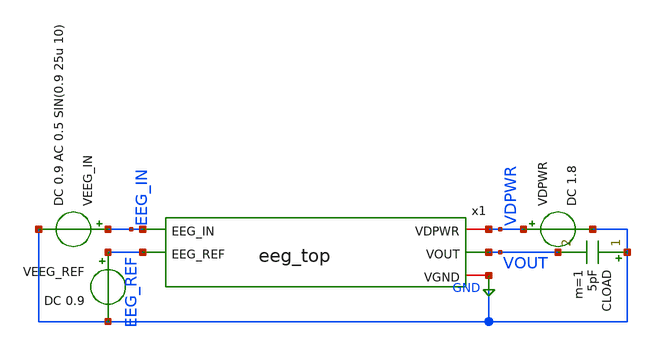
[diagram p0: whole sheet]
** sch_path: xschem/tb_eeg_top.sch
**.subckt tb_eeg_top
VDPWR VDPWR GND DC 1.8
VEEG_REF EEG_REF GND DC 0.9
VEEG_IN EEG_IN GND DC 0.9 AC 0.5 SIN(0.9 25u 10)
CLOAD GND VOUT 5pF m=1
x1 VDPWR EEG_IN VOUT GND EEG_REF eeg_top
**** begin user architecture code


.lib /foss/pdks/sky130A/libs.tech/ngspice/sky130.lib.spice tt_mm

.ic v(VOUT)=0.5 v(x1.ota_inp)=0.5 v(x1.ota_inn)=0.5    v(x1.x_ota.tail_p)=1.5 v(x1.x_ota.EEG_IN)=0.5
+    v(x1.x_rpseudo_p.EEG_IN)=0.5 v(x1.x_rpseudo_fb.EEG_IN)=0.5

.nodeset v(VOUT)=0.5 v(x1.ota_inp)=0.5 v(x1.ota_inn)=0.5         v(x1.x_ota.tail_p)=1.5
+ v(x1.x_ota.EEG_IN)=0.5         v(x1.x_rpseudo_p.EEG_IN)=0.5 v(x1.x_rpseudo_fb.EEG_IN)=0.5

.option savecurrents
.option rshunt=1e15
.option gmin=1e-15
.option method=gear
.option cshunt=1e-15

.control
op
echo ===== Bias Verification =====
print @m.x1.x_ota.xmtail[id]
print v(x1.x_ota.tail_p)
print v(x1.bias_p)
print @m.x1.x_ota.xmdiff_p[id]
print @m.x1.x_ota.xmdiff_n[id]

echo ===== Operating Point =====
print v(x1.ota_inp)
print v(x1.ota_inn)
print v(x1.ota_inp)-v(x1.ota_inn)
print v(VOUT)

echo ===== Transient =====
tran 1m 20
plot v(EEG_IN)
plot v(x1.ota_inp)
plot v(x1.ota_inn)
plot v(x1.ota_inp)-v(x1.ota_inn)
plot v(VOUT)
plot v(VOUT)-0.84

echo ===== Noise =====
noise v(VOUT) veeg_in dec 100 0.5 100

* Active plot is the totals plot — print integrated values
print inoise_total
print onoise_total

* Switch to the spectrum plot to see vs frequency
setplot previous
plot db(inoise_spectrum)
plot db(onoise_spectrum)

echo ===== AC =====
ac dec 100 0.01 100k
plot db(v(VOUT)/v(EEG_IN))

plot db(v(x1.ota_inp)/v(EEG_IN))
plot db(v(x1.ota_inn)/v(EEG_REF))
plot db(v(VOUT)/(v(x1.ota_inp)-v(x1.ota_inn)))

.endc


**** end user architecture code
**.ends

* expanding   symbol:  eeg_top.sym # of pins=5
** sym_path: xschem/eeg_top.sym
** sch_path: xschem/eeg_top.sch
.subckt eeg_top VDPWR EEG_IN VOUT VGND EEG_REF
*.ipin EEG_IN
*.ipin EEG_REF
*.iopin VDPWR
*.iopin VGND
*.opin VOUT
x1 BIAS_P VDPWR OTA_INP OTA_INN VOUT VGND ota_5t
x2 VDPWR BIAS_VCM OTA_INN pseudo_res_c
x3 BIAS_P VGND VDPWR bias_gen
x4 VDPWR BIAS_VCM OTA_INP pseudo_res_c
Cf2 VOUT OTA_INN 1p m=1
Cf1 VOUT OTA_INP 1p m=1
Cin1 OTA_INP EEG_IN 10p m=1
Cin2 OTA_INN EEG_REF 10p m=1
xVCM_GEN BIAS_VCM VGND VDPWR bias_gen
.ends


* expanding   symbol:  ota_5t.sym # of pins=6
** sym_path: xschem-new/ota_5t.sym
** sch_path: xschem-new/ota_5t.sch
.subckt ota_5t BIAS_P VDPWR VIN_P VIN_N VOUT VGND
*.ipin VIN_P
*.ipin VIN_N
*.ipin BIAS_P
*.iopin VDPWR
*.iopin VGND
*.opin VOUT
XMDIFF_P net1 VIN_P TAIL_P VDPWR sky130_fd_pr__pfet_01v8 L=4 W=48 nf=1 ad='int((1 + 1)/2) * 48 / 1 * 0.29'
+ as='int((1 + 2)/2) * 48 / 1 * 0.29' pd='2*int((1 + 1)/2) * (48 / 1 + 0.29)' ps='2*int((1 + 2)/2) * (48 / 1 + 0.29)'
+ nrd='0.29 / 48 ' nrs='0.29 / 48 ' sa=0 sb=0 sd=0 mult=1 m=1
XMDIFF_N VOUT VIN_N TAIL_P VDPWR sky130_fd_pr__pfet_01v8 L=4 W=48 nf=1 ad='int((1 + 1)/2) * 48 / 1 * 0.29'
+ as='int((1 + 2)/2) * 48 / 1 * 0.29' pd='2*int((1 + 1)/2) * (48 / 1 + 0.29)' ps='2*int((1 + 2)/2) * (48 / 1 + 0.29)'
+ nrd='0.29 / 48 ' nrs='0.29 / 48 ' sa=0 sb=0 sd=0 mult=1 m=1
XMTAIL TAIL_P BIAS_P VDPWR VDPWR sky130_fd_pr__pfet_01v8 L=8 W=0.5 nf=1 ad='int((1 + 1)/2) * 0.5 / 1 * 0.29'
+ as='int((1 + 2)/2) * 0.5 / 1 * 0.29' pd='2*int((1 + 1)/2) * (0.5 / 1 + 0.29)' ps='2*int((1 + 2)/2) * (0.5 / 1 + 0.29)'
+ nrd='0.29 / 0.5 ' nrs='0.29 / 0.5 ' sa=0 sb=0 sd=0 mult=1 m=1
XMLOAD_REF net1 net1 VGND VGND sky130_fd_pr__nfet_01v8 L=16 W=8 nf=1 ad='int((1 + 1)/2) * 8 / 1 * 0.29'
+ as='int((1 + 2)/2) * 8 / 1 * 0.29' pd='2*int((1 + 1)/2) * (8 / 1 + 0.29)' ps='2*int((1 + 2)/2) * (8 / 1 + 0.29)'
+ nrd='0.29 / 8 ' nrs='0.29 / 8 ' sa=0 sb=0 sd=0 mult=1 m=1
XMLOAD_OUT VOUT net1 VGND VGND sky130_fd_pr__nfet_01v8 L=16 W=8 nf=1 ad='int((1 + 1)/2) * 8 / 1 * 0.29'
+ as='int((1 + 2)/2) * 8 / 1 * 0.29' pd='2*int((1 + 1)/2) * (8 / 1 + 0.29)' ps='2*int((1 + 2)/2) * (8 / 1 + 0.29)'
+ nrd='0.29 / 8 ' nrs='0.29 / 8 ' sa=0 sb=0 sd=0 mult=1 m=1
.ends


* expanding   symbol:  pseudo_res_c.sym # of pins=3
** sym_path: xschem/pseudo_res_c.sym
** sch_path: xschem/pseudo_res_c.sch
.subckt pseudo_res_c VDPWR B A
*.iopin A
*.iopin B
*.iopin VDPWR
XP1 A net1 net1 VDPWR sky130_fd_pr__pfet_01v8 L=5 W=0.5 nf=1 ad='int((1 + 1)/2) * 0.5 / 1 * 0.29' as='int((1 + 2)/2) * 0.5 / 1 * 0.29'
+ pd='2*int((1 + 1)/2) * (0.5 / 1 + 0.29)' ps='2*int((1 + 2)/2) * (0.5 / 1 + 0.29)' nrd='0.29 / 0.5 ' nrs='0.29 / 0.5 '
+ sa=0 sb=0 sd=0 mult=10 m=10
XP2 net1 net1 B VDPWR sky130_fd_pr__pfet_01v8 L=5 W=0.5 nf=1 ad='int((1 + 1)/2) * 0.5 / 1 * 0.29' as='int((1 + 2)/2) * 0.5 / 1 * 0.29'
+ pd='2*int((1 + 1)/2) * (0.5 / 1 + 0.29)' ps='2*int((1 + 2)/2) * (0.5 / 1 + 0.29)' nrd='0.29 / 0.5 ' nrs='0.29 / 0.5 '
+ sa=0 sb=0 sd=0 mult=10 m=10
.ends


* expanding   symbol:  bias_gen.sym # of pins=3
** sym_path: xschem/bias_gen.sym
** sch_path: xschem/bias_gen.sch
.subckt bias_gen BIAS_P VGND VDPWR
*.iopin VDPWR
*.iopin VGND
*.opin BIAS_P
XM_BIAS_P BIAS_P BIAS_P VDPWR VDPWR sky130_fd_pr__pfet_01v8 L=2 W=1 nf=1 ad='int((1 + 1)/2) * 1 / 1 * 0.29'
+ as='int((1 + 2)/2) * 1 / 1 * 0.29' pd='2*int((1 + 1)/2) * (1 / 1 + 0.29)' ps='2*int((1 + 2)/2) * (1 / 1 + 0.29)'
+ nrd='0.29 / 1 ' nrs='0.29 / 1 ' sa=0 sb=0 sd=0 mult=1 m=1
XM_BIAS_N BIAS_P BIAS_P VGND VGND sky130_fd_pr__nfet_01v8 L=2 W=0.5 nf=1 ad='int((1 + 1)/2) * 0.5 / 1 * 0.29'
+ as='int((1 + 2)/2) * 0.5 / 1 * 0.29' pd='2*int((1 + 1)/2) * (0.5 / 1 + 0.29)' ps='2*int((1 + 2)/2) * (0.5 / 1 + 0.29)'
+ nrd='0.29 / 0.5 ' nrs='0.29 / 0.5 ' sa=0 sb=0 sd=0 mult=1 m=1
.ends

.GLOBAL GND
.end
